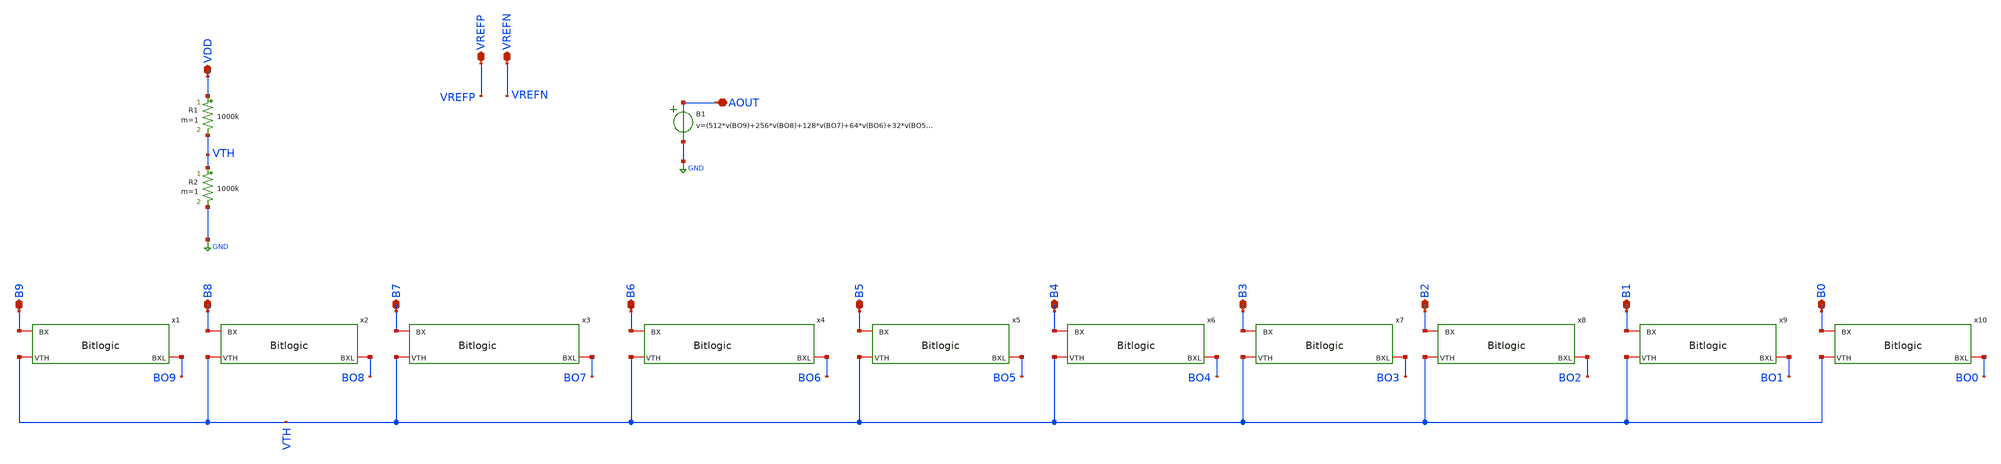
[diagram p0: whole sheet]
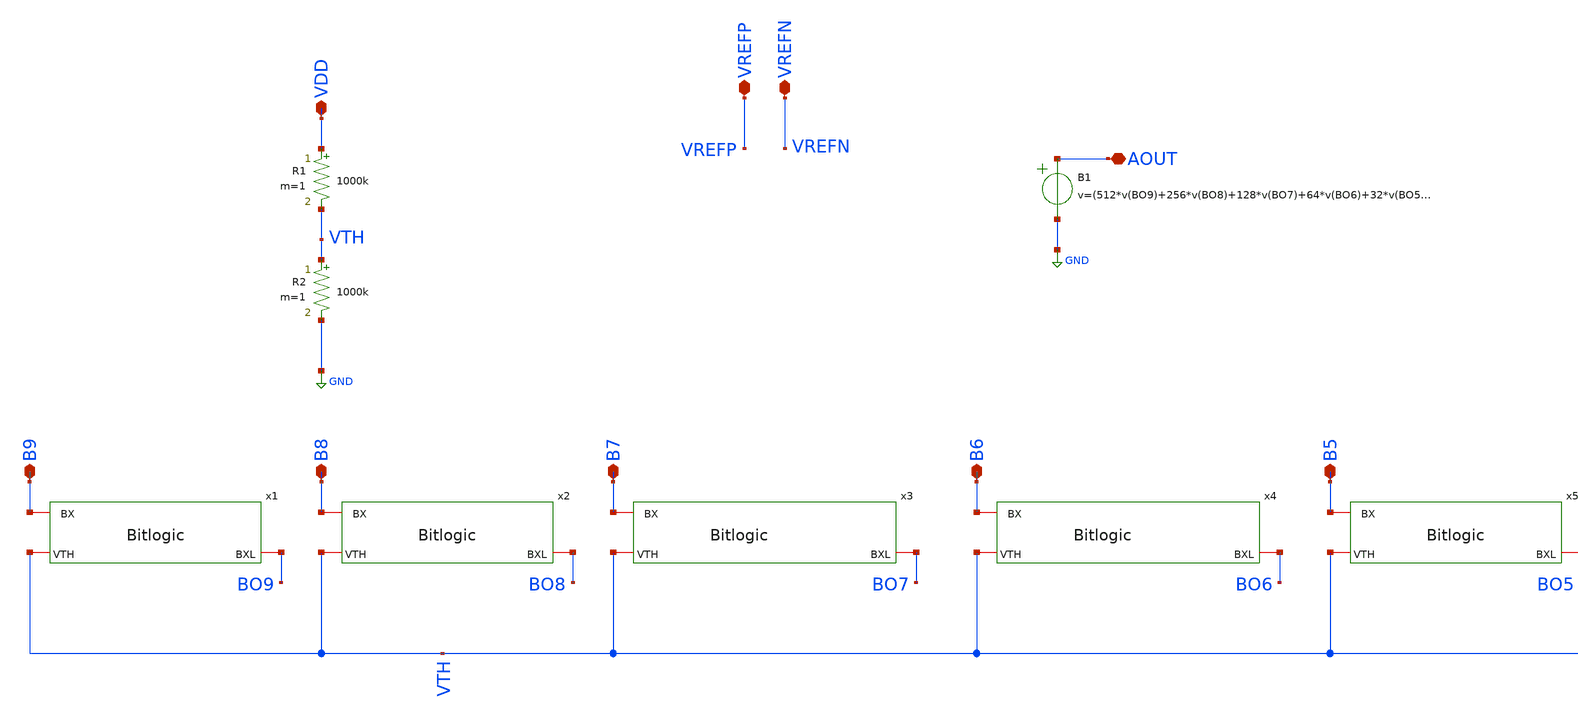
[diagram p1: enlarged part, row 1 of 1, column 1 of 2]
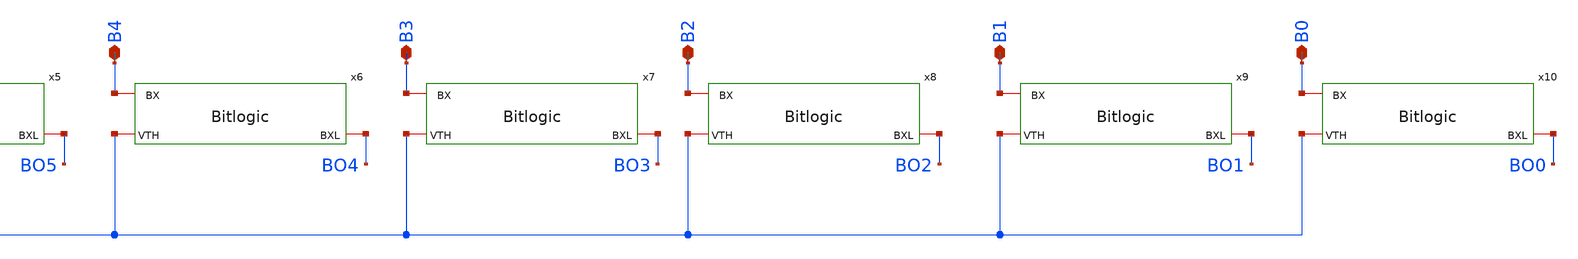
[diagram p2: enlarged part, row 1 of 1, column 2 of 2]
** sch_path: Designs/DAC_10.sch
**.subckt DAC_10 VDD B9 B8 B7 B6 B5 B4 B3 B2 B1 B0 VREFP VREFN AOUT
*.iopin VDD
*.iopin B9
*.iopin B8
*.iopin B7
*.iopin B6
*.iopin B5
*.iopin B4
*.iopin B3
*.iopin B2
*.iopin B1
*.iopin B0
*.iopin VREFP
*.iopin VREFN
*.iopin AOUT
x1 VTH B9 BO9 Bitlogic
x2 VTH B8 BO8 Bitlogic
x3 VTH B7 BO7 Bitlogic
x4 VTH B6 BO6 Bitlogic
x5 VTH B5 BO5 Bitlogic
x6 VTH B4 BO4 Bitlogic
x7 VTH B3 BO3 Bitlogic
x8 VTH B2 BO2 Bitlogic
x9 VTH B1 BO1 Bitlogic
x10 VTH B0 BO0 Bitlogic
R1 VDD VTH 1000k m=1
R2 VTH GND 1000k m=1
B1 AOUT GND
+ v=(512*v(BO9)+256*v(BO8)+128*v(BO7)+64*v(BO6)+32*v(BO5)+16*v(BO4)+8*v(BO3)+4*v(BO2)+2*v(BO1)+v(BO0))*((v(VREFP)-v(VREFN))/1024)+v(VREFN)
**.ends
.GLOBAL GND
.end
